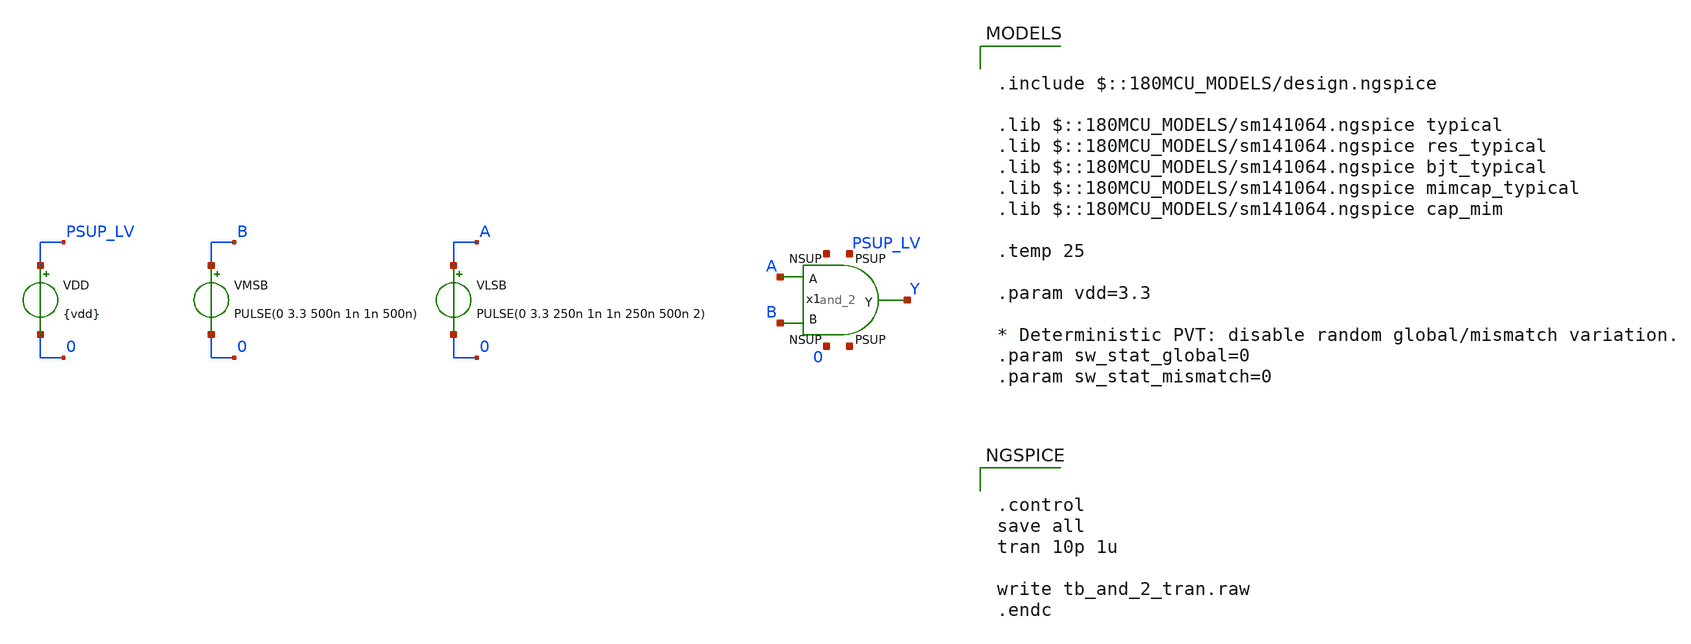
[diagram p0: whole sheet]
** sch_path: xschem/blocks/and_2/tb_and_2_tran.sch
**.subckt tb_and_2_tran
VLSB A 0 PULSE(0 3.3 250n 1n 1n 250n 500n 2)
VMSB B 0 PULSE(0 3.3 500n 1n 1n 500n)
VDD PSUP_LV 0 {vdd}
x1 Y A B PSUP_LV 0 and_2
**** begin user architecture code

.include $::180MCU_MODELS/design.ngspice

.lib $::180MCU_MODELS/sm141064.ngspice typical
.lib $::180MCU_MODELS/sm141064.ngspice res_typical
.lib $::180MCU_MODELS/sm141064.ngspice bjt_typical
.lib $::180MCU_MODELS/sm141064.ngspice mimcap_typical
.lib $::180MCU_MODELS/sm141064.ngspice cap_mim

.temp 25

.param vdd=3.3

* Deterministic PVT: disable random global/mismatch variation.
.param sw_stat_global=0
.param sw_stat_mismatch=0



.control
save all
tran 10p 1u

write tb_and_2_tran.raw
.endc


**** end user architecture code
**.ends

* expanding   symbol:  blocks/and_2/and_2.sym # of pins=7
** sym_path: xschem/blocks/and_2/and_2.sym
** sch_path: xschem/blocks/and_2/and_2.sch
.subckt and_2 Y A B PSUP NSUP
*.ipin PSUP
*.ipin NSUP
*.ipin A
*.ipin B
*.opin Y
x1 net1 A B PSUP NSUP nand_2
x2 PSUP net1 Y NSUP not
.ends


* expanding   symbol:  blocks/nand_2/nand_2.sym # of pins=7
** sym_path: xschem/blocks/nand_2/nand_2.sym
** sch_path: xschem/blocks/nand_2/nand_2.sch
.subckt nand_2 Y A B PSUP NSUP
*.ipin PSUP
*.ipin NSUP
*.ipin A
*.ipin B
*.opin Y
XM5 net1 B NSUP NSUP nfet_03v3 L=0.28u W=0.22u nf=1 ad='int((nf+1)/2) * W/nf * 0.18u' as='int((nf+2)/2) * W/nf * 0.18u'
+ pd='2*int((nf+1)/2) * (W/nf + 0.18u)' ps='2*int((nf+2)/2) * (W/nf + 0.18u)' nrd='0.18u / W' nrs='0.18u / W'
+ sa=0 sb=0 sd=0 m=1
XM1 Y A net1 NSUP nfet_03v3 L=0.28u W=0.22u nf=1 ad='int((nf+1)/2) * W/nf * 0.18u' as='int((nf+2)/2) * W/nf * 0.18u'
+ pd='2*int((nf+1)/2) * (W/nf + 0.18u)' ps='2*int((nf+2)/2) * (W/nf + 0.18u)' nrd='0.18u / W' nrs='0.18u / W'
+ sa=0 sb=0 sd=0 m=1
XM2 Y A PSUP PSUP pfet_03v3 L=0.28u W=0.5u nf=1 ad='int((nf+1)/2) * W/nf * 0.18u' as='int((nf+2)/2) * W/nf * 0.18u'
+ pd='2*int((nf+1)/2) * (W/nf + 0.18u)' ps='2*int((nf+2)/2) * (W/nf + 0.18u)' nrd='0.18u / W' nrs='0.18u / W'
+ sa=0 sb=0 sd=0 m=1
XM3 Y B PSUP PSUP pfet_03v3 L=0.28u W=0.5u nf=1 ad='int((nf+1)/2) * W/nf * 0.18u' as='int((nf+2)/2) * W/nf * 0.18u'
+ pd='2*int((nf+1)/2) * (W/nf + 0.18u)' ps='2*int((nf+2)/2) * (W/nf + 0.18u)' nrd='0.18u / W' nrs='0.18u / W'
+ sa=0 sb=0 sd=0 m=1
.ends


* expanding   symbol:  blocks/not/not.sym # of pins=6
** sym_path: xschem/blocks/not/not.sym
** sch_path: xschem/blocks/not/not.sch
.subckt not PSUP A B NSUP
*.ipin PSUP
*.ipin NSUP
*.ipin A
*.opin B
XM2 B A NSUP NSUP nfet_03v3 L=0.28u W=0.22u nf=1 ad='int((nf+1)/2) * W/nf * 0.18u' as='int((nf+2)/2) * W/nf * 0.18u'
+ pd='2*int((nf+1)/2) * (W/nf + 0.18u)' ps='2*int((nf+2)/2) * (W/nf + 0.18u)' nrd='0.18u / W' nrs='0.18u / W'
+ sa=0 sb=0 sd=0 m=1
XM1 B A PSUP PSUP pfet_03v3 L=0.28u W=0.5u nf=1 ad='int((nf+1)/2) * W/nf * 0.18u' as='int((nf+2)/2) * W/nf * 0.18u'
+ pd='2*int((nf+1)/2) * (W/nf + 0.18u)' ps='2*int((nf+2)/2) * (W/nf + 0.18u)' nrd='0.18u / W' nrs='0.18u / W'
+ sa=0 sb=0 sd=0 m=1
.ends

.end
